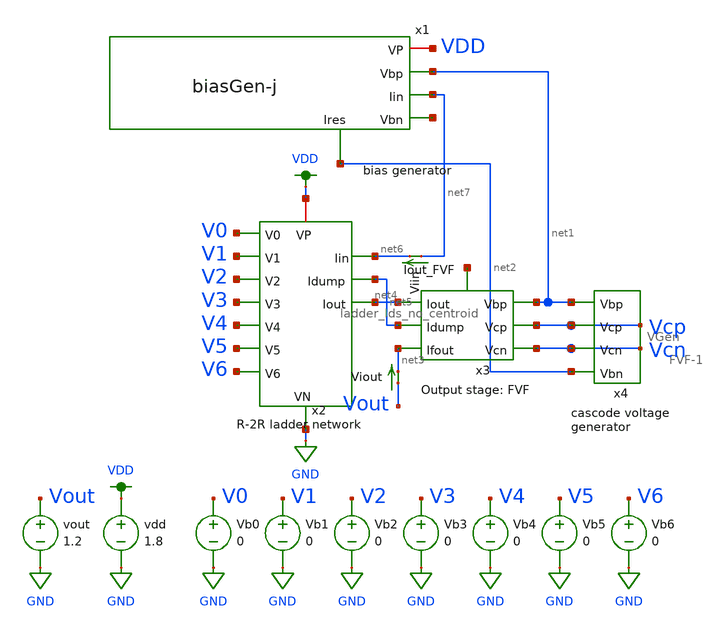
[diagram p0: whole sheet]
** sch_path: xschem/new_sim_cascode_ladder_lds_no_centroid.sch
**.subckt new_sim_cascode_ladder_lds_no_centroid
Vb1 V1 GND 0
Vb2 V2 GND 0
Vb3 V3 GND 0
Vb4 V4 GND 0
Vb5 V5 GND 0
Vb6 V6 GND 0
Vb0 V0 GND 0
x3 net1 Vcp net4 Vcn net3 net5 net8 FVF-1
x4 net1 Vcn Vcp net2 VGen
vdd VDD GND 1.8
vout Vout GND 1.2
Viout Vout net3 0
.save i(viout)
Viin net7 net6 0
.save i(viin)
x1 VDD net1 net7 net9 net2 biasGen-j
x2 V0 VDD net5 net4 net6 V1 V2 V3 V4 V5 V6 GND ladder_lds_no_centroid
**** begin user architecture code

.option wnflag=1
.param MC_SWITCH=1.0
.lib ~/skywater/skywater-pdk/libraries/sky130_fd_pr_ngspice/latest/models/sky130.lib.spice tt



.control
  set wr_singlescale
let runs = 10
  let run = 1
	while run <= runs
 set appendwrite = FALSE
  set wr_vecnames
  let code = 0
  while code < 128
    if code eq 0
      let b0 = 0
    else
      let b0 = code % 2
    end
    if floor(code / 2) eq 0
      let b1 = 0
    else
      let b1 = floor(code / 2) % 2
    end
    if floor(code / 4) eq 0
      let b2 = 0
    else
      let b2 = floor(code / 4) % 2
    end
    if floor(code / 8) eq 0
      let b3 = 0
    else
      let b3 = floor(code / 8) % 2
    end
    if floor(code / 16) eq 0
      let b4 = 0
    else
      let b4 = floor(code / 16) % 2
    end
    if floor(code / 32) eq 0
      let b5 = 0
    else
      let b5 = floor(code / 32) % 2
    end
    if floor(code / 64) eq 0
      let b6 = 0
    else
      let b6 = floor(code / 64) % 2
    end
    alter Vb0 1.8*$&b0
    alter Vb1 1.8*$&b1
    alter Vb2 1.8*$&b2
    alter Vb3 1.8*$&b3
    alter Vb4 1.8*$&b4
    alter Vb5 1.8*$&b5
    alter Vb6 1.8*$&b6
    save all
    op
    wrdata ~/Documents/DAC-VLSI/simulation_results/mc/24_8_ladder_lds_no_centroid_{$&run}.txt i(Viin)
+ i(Viout)
    if code eq 0
      set appendwrite
      set wr_vecnames = FALSE
    end
    let code = code + 1
  end
reset
let run = run + 1
end
  quit
.endc

**** end user architecture code
**.ends
.GLOBAL GND
.GLOBAL VDD
.end
